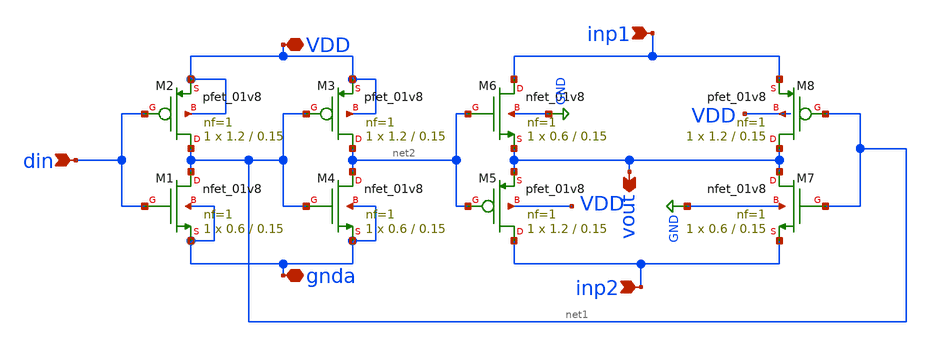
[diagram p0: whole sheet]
** sch_path: week7/pre-layout/switch.sch
**.subckt switch din VDD inp1 inp2 gnda vout
*.ipin din
*.iopin VDD
*.ipin inp1
*.ipin inp2
*.iopin gnda
*.opin vout
XM1 net1 din gnda gnda sky130_fd_pr__nfet_01v8 L=0.15 W=0.6 nf=1 ad='int((nf+1)/2) * W/nf * 0.29' as='int((nf+2)/2) * W/nf * 0.29'
+ pd='2*int((nf+1)/2) * (W/nf + 0.29)' ps='2*int((nf+2)/2) * (W/nf + 0.29)' nrd='0.29 / W' nrs='0.29 / W'
+ sa=0 sb=0 sd=0 mult=1 m=1
XM2 net1 din VDD VDD sky130_fd_pr__pfet_01v8 L=0.15 W=1.2 nf=1 ad='int((nf+1)/2) * W/nf * 0.29' as='int((nf+2)/2) * W/nf * 0.29'
+ pd='2*int((nf+1)/2) * (W/nf + 0.29)' ps='2*int((nf+2)/2) * (W/nf + 0.29)' nrd='0.29 / W' nrs='0.29 / W'
+ sa=0 sb=0 sd=0 mult=1 m=1
XM3 net2 net1 VDD VDD sky130_fd_pr__pfet_01v8 L=0.15 W=1.2 nf=1 ad='int((nf+1)/2) * W/nf * 0.29' as='int((nf+2)/2) * W/nf * 0.29'
+ pd='2*int((nf+1)/2) * (W/nf + 0.29)' ps='2*int((nf+2)/2) * (W/nf + 0.29)' nrd='0.29 / W' nrs='0.29 / W'
+ sa=0 sb=0 sd=0 mult=1 m=1
XM4 net2 net1 gnda gnda sky130_fd_pr__nfet_01v8 L=0.15 W=0.6 nf=1 ad='int((nf+1)/2) * W/nf * 0.29' as='int((nf+2)/2) * W/nf * 0.29'
+ pd='2*int((nf+1)/2) * (W/nf + 0.29)' ps='2*int((nf+2)/2) * (W/nf + 0.29)' nrd='0.29 / W' nrs='0.29 / W'
+ sa=0 sb=0 sd=0 mult=1 m=1
XM5 inp2 net2 vout VDD sky130_fd_pr__pfet_01v8 L=0.15 W=1.2 nf=1 ad='int((nf+1)/2) * W/nf * 0.29' as='int((nf+2)/2) * W/nf * 0.29'
+ pd='2*int((nf+1)/2) * (W/nf + 0.29)' ps='2*int((nf+2)/2) * (W/nf + 0.29)' nrd='0.29 / W' nrs='0.29 / W'
+ sa=0 sb=0 sd=0 mult=1 m=1
XM6 inp1 net2 vout GND sky130_fd_pr__nfet_01v8 L=0.15 W=0.6 nf=1 ad='int((nf+1)/2) * W/nf * 0.29' as='int((nf+2)/2) * W/nf * 0.29'
+ pd='2*int((nf+1)/2) * (W/nf + 0.29)' ps='2*int((nf+2)/2) * (W/nf + 0.29)' nrd='0.29 / W' nrs='0.29 / W'
+ sa=0 sb=0 sd=0 mult=1 m=1
XM7 vout net1 inp2 GND sky130_fd_pr__nfet_01v8 L=0.15 W=0.6 nf=1 ad='int((nf+1)/2) * W/nf * 0.29' as='int((nf+2)/2) * W/nf * 0.29'
+ pd='2*int((nf+1)/2) * (W/nf + 0.29)' ps='2*int((nf+2)/2) * (W/nf + 0.29)' nrd='0.29 / W' nrs='0.29 / W'
+ sa=0 sb=0 sd=0 mult=1 m=1
XM8 vout net1 inp1 VDD sky130_fd_pr__pfet_01v8 L=0.15 W=1.2 nf=1 ad='int((nf+1)/2) * W/nf * 0.29' as='int((nf+2)/2) * W/nf * 0.29'
+ pd='2*int((nf+1)/2) * (W/nf + 0.29)' ps='2*int((nf+2)/2) * (W/nf + 0.29)' nrd='0.29 / W' nrs='0.29 / W'
+ sa=0 sb=0 sd=0 mult=1 m=1
**.ends
.GLOBAL GND
.end
